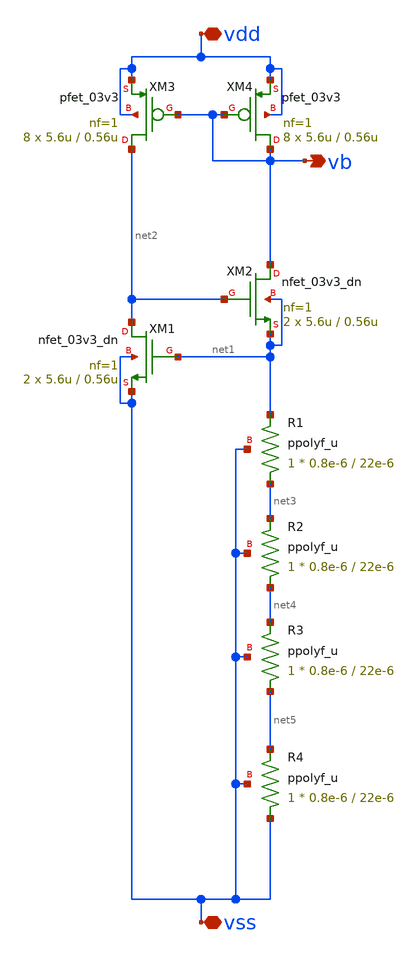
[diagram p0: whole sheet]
** sch_path: maple0705/SAR_ADC/xschem/cs_vthref_lvs.sch
**.subckt cs_vthref_lvs vss vdd vb
*.iopin vss
*.iopin vdd
*.opin vb
XM4 vb vb vdd vdd pfet_03v3 L=0.56u W=5.6u nf=1 ad='int((nf+1)/2) * W/nf * 0.18u' as='int((nf+2)/2) * W/nf * 0.18u'
+ pd='2*int((nf+1)/2) * (W/nf + 0.18u)' ps='2*int((nf+2)/2) * (W/nf + 0.18u)' nrd='0.18u / W' nrs='0.18u / W'
+ sa=0 sb=0 sd=0 m=8
XM3 net2 vb vdd vdd pfet_03v3 L=0.56u W=5.6u nf=1 ad='int((nf+1)/2) * W/nf * 0.18u' as='int((nf+2)/2) * W/nf * 0.18u'
+ pd='2*int((nf+1)/2) * (W/nf + 0.18u)' ps='2*int((nf+2)/2) * (W/nf + 0.18u)' nrd='0.18u / W' nrs='0.18u / W'
+ sa=0 sb=0 sd=0 m=8
XM2 vb net2 net1 net1 nfet_03v3_dn L=0.56u W=5.6u nf=1 ad='int((nf+1)/2) * W/nf * 0.18u' as='int((nf+2)/2) * W/nf * 0.18u'
+ pd='2*int((nf+1)/2) * (W/nf + 0.18u)' ps='2*int((nf+2)/2) * (W/nf + 0.18u)' nrd='0.18u / W' nrs='0.18u / W'
+ sa=0 sb=0 sd=0 m=2
XM1 net2 net1 vss vss nfet_03v3_dn L=0.56u W=5.6u nf=1 ad='int((nf+1)/2) * W/nf * 0.18u' as='int((nf+2)/2) * W/nf * 0.18u'
+ pd='2*int((nf+1)/2) * (W/nf + 0.18u)' ps='2*int((nf+2)/2) * (W/nf + 0.18u)' nrd='0.18u / W' nrs='0.18u / W'
+ sa=0 sb=0 sd=0 m=2
R1 net3 net1 vss ppolyf_u W=0.8e-6 L=22e-6 m=1
R2 net4 net3 vss ppolyf_u W=0.8e-6 L=22e-6 m=1
R3 net5 net4 vss ppolyf_u W=0.8e-6 L=22e-6 m=1
R4 vss net5 vss ppolyf_u W=0.8e-6 L=22e-6 m=1
**.ends
.end
